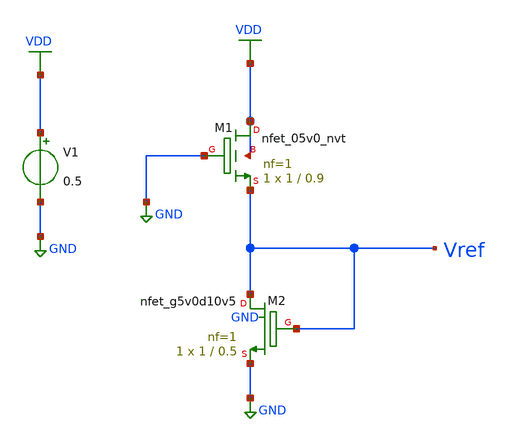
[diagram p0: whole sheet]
** sch_path: 2TBGR/Schematics/bgr1try.sch
**.subckt bgr1try
XM1 VDD GND Vref VDD sky130_fd_pr__nfet_05v0_nvt L=0.9 W=1 nf=1 ad='int((nf+1)/2) * W/nf * 0.29' as='int((nf+2)/2) * W/nf * 0.29'
+ pd='2*int((nf+1)/2) * (W/nf + 0.29)' ps='2*int((nf+2)/2) * (W/nf + 0.29)' nrd='0.29 / W' nrs='0.29 / W'
+ sa=0 sb=0 sd=0 mult=1 m=1
XM2 Vref Vref GND GND sky130_fd_pr__nfet_g5v0d10v5 L=0.5 W=1 nf=1 ad='int((nf+1)/2) * W/nf * 0.29' as='int((nf+2)/2) * W/nf * 0.29'
+ pd='2*int((nf+1)/2) * (W/nf + 0.29)' ps='2*int((nf+2)/2) * (W/nf + 0.29)' nrd='0.29 / W' nrs='0.29 / W'
+ sa=0 sb=0 sd=0 mult=1 m=1
V1 VDD GND 0.5
**.ends
.GLOBAL GND
.GLOBAL VDD
.end
